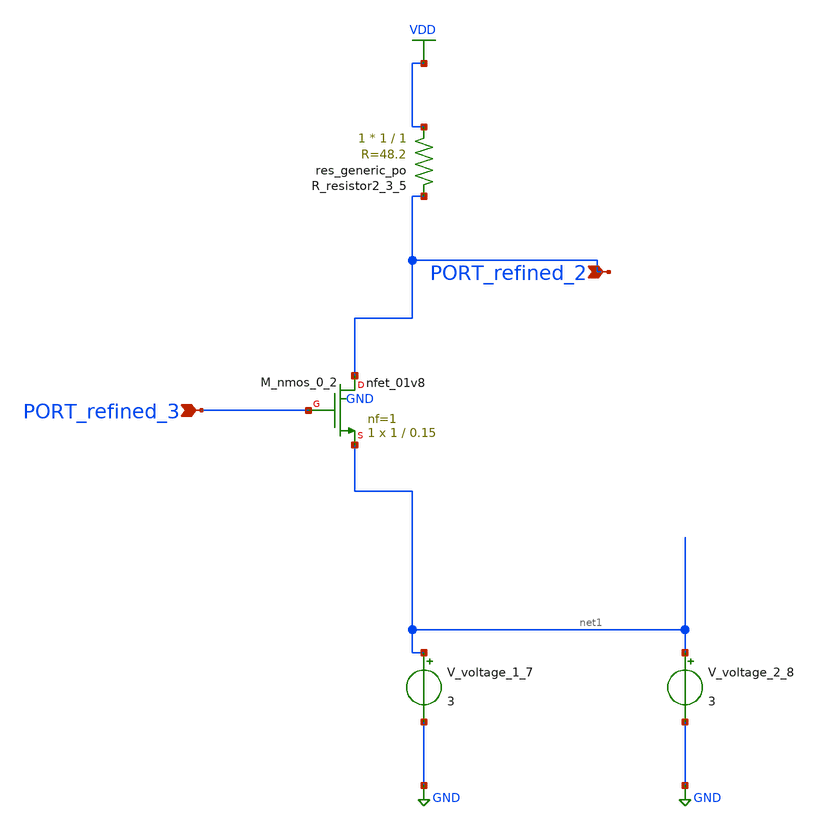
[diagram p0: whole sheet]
** sch_path: schematics/AMSNet/39.sch
**.subckt 39 PORT_refined_3 PORT_refined_2
*.ipin PORT_refined_3
*.ipin PORT_refined_2
XM_nmos_0_2 PORT_refined_2 PORT_refined_3 net1 GND sky130_fd_pr__nfet_01v8 L=0.15 W=1 nf=1 ad='int((1 + 1)/2) * 1 / 1 * 0.29'
+ as='int((1 + 2)/2) * 1 / 1 * 0.29' pd='2*int((1 + 1)/2) * (1 / 1 + 0.29)' ps='2*int((1 + 2)/2) * (1 / 1 + 0.29)'
+ nrd='0.29 / 1 ' nrs='0.29 / 1 ' sa=0 sb=0 sd=0 mult=1 m=1
XR_resistor2_3_5 VDD PORT_refined_2 sky130_fd_pr__res_generic_po W=1 L=1 m=1
V_voltage_1_7 net1 GND 3
V_voltage_2_8 net1 GND 3
**.ends
.GLOBAL GND
.GLOBAL VDD
.end
